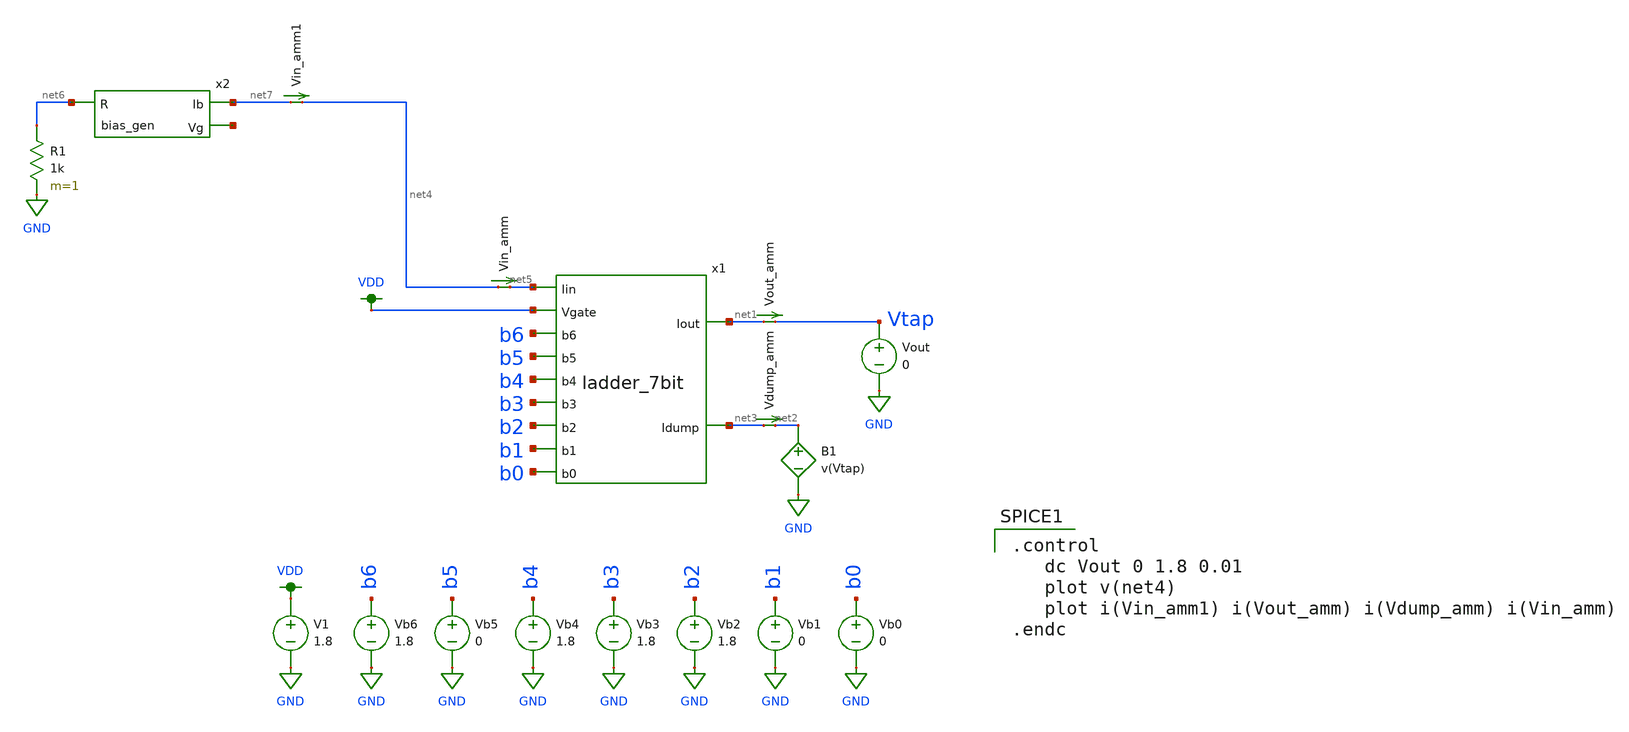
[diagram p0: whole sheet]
** sch_path: test_harness_dcvout.sch
**.subckt test_harness_dcvout
Vb0 b0 GND 0
Vb1 b1 GND 0
Vb2 b2 GND 1.8
Vb3 b3 GND 1.8
Vb4 b4 GND 1.8
Vb5 b5 GND 0
Vb6 b6 GND 1.8
Vout Vtap GND 0
Vout_amm net1 Vtap 0
.save i(vout_amm)
Vdump_amm net3 net2 0
.save i(vdump_amm)
x1 VDD net5 net3 net1 b5 b4 b1 b2 b3 b0 b6 ladder_7bit
Vin_amm net4 net5 0
.save i(vin_amm)
x2 net7 net8 net6 bias_gen
R1 net6 GND 1k m=1
Vin_amm1 net7 net4 0
.save i(vin_amm1)
B1 net2 GND V=v(Vtap)
V1 VDD GND 1.8
**** begin user architecture code

.control
   dc Vout 0 1.8 0.01
   plot v(net4)
   plot i(Vin_amm1) i(Vout_amm) i(Vdump_amm) i(Vin_amm)
.endc


.option wnflag=1
.param MC_SWITCH=0.0
.lib ~/skywater/skywater-pdk/libraries/sky130_fd_pr_ngspice/latest/models/sky130.lib.spice tt

**** end user architecture code
**.ends
.GLOBAL GND
.GLOBAL VDD
.end
